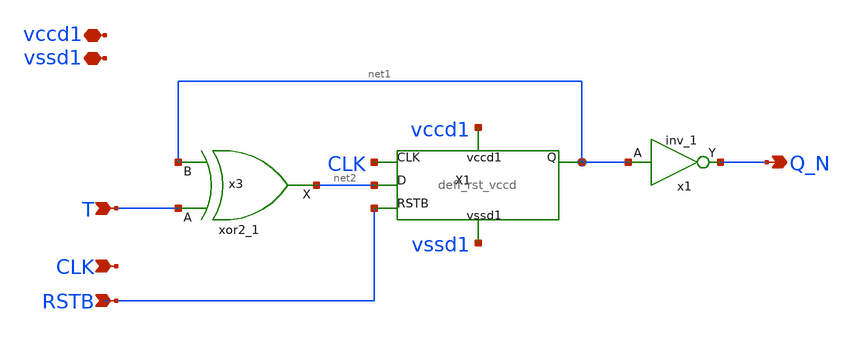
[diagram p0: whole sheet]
** sch_path: xschem/digital/asyn_rst_t_ff_vccd.sch
**.subckt asyn_rst_t_ff_vccd T CLK Q_N RSTB vccd1 vssd1
*.ipin T
*.ipin CLK
*.opin Q_N
*.ipin RSTB
*.iopin vccd1
*.iopin vssd1
x3 T net1 vssd1 vssd1 vccd1 vccd1 net2 sky130_fd_sc_hd__xor2_1
x1 net1 vssd1 vssd1 vccd1 vccd1 Q_N sky130_fd_sc_hd__inv_1
X1 CLK net2 net1 RSTB vccd1 vssd1 deff_rst_vccd
**.ends

* expanding   symbol:  digital/deff_rst_vccd.sym # of pins=6
** sym_path: xschem/digital/deff_rst_vccd.sym
** sch_path: xschem/digital/deff_rst_vccd.sch
.subckt deff_rst_vccd CLK D Q RSTB vccd1 vssd1
*.ipin CLK
*.ipin D
*.opin Q
*.ipin RSTB
*.iopin vccd1
*.iopin vssd1
x3 net1 net2 net3 vssd1 vssd1 vccd1 vccd1 Q sky130_fd_sc_hd__mux2_1
x21 CLK D RSTB vssd1 vssd1 vccd1 vccd1 net1 sky130_fd_sc_hd__dfrtn_1
x1 CLK D RSTB vssd1 vssd1 vccd1 vccd1 net2 sky130_fd_sc_hd__dfrtp_1
x17 net4 vssd1 vssd1 vccd1 vccd1 net5 sky130_fd_sc_hd__buf_1
x2 net5 vssd1 vssd1 vccd1 vccd1 net3 sky130_fd_sc_hd__buf_1
x4 CLK vssd1 vssd1 vccd1 vccd1 net6 sky130_fd_sc_hd__buf_1
x5 net6 vssd1 vssd1 vccd1 vccd1 net4 sky130_fd_sc_hd__buf_1
.ends

.end
